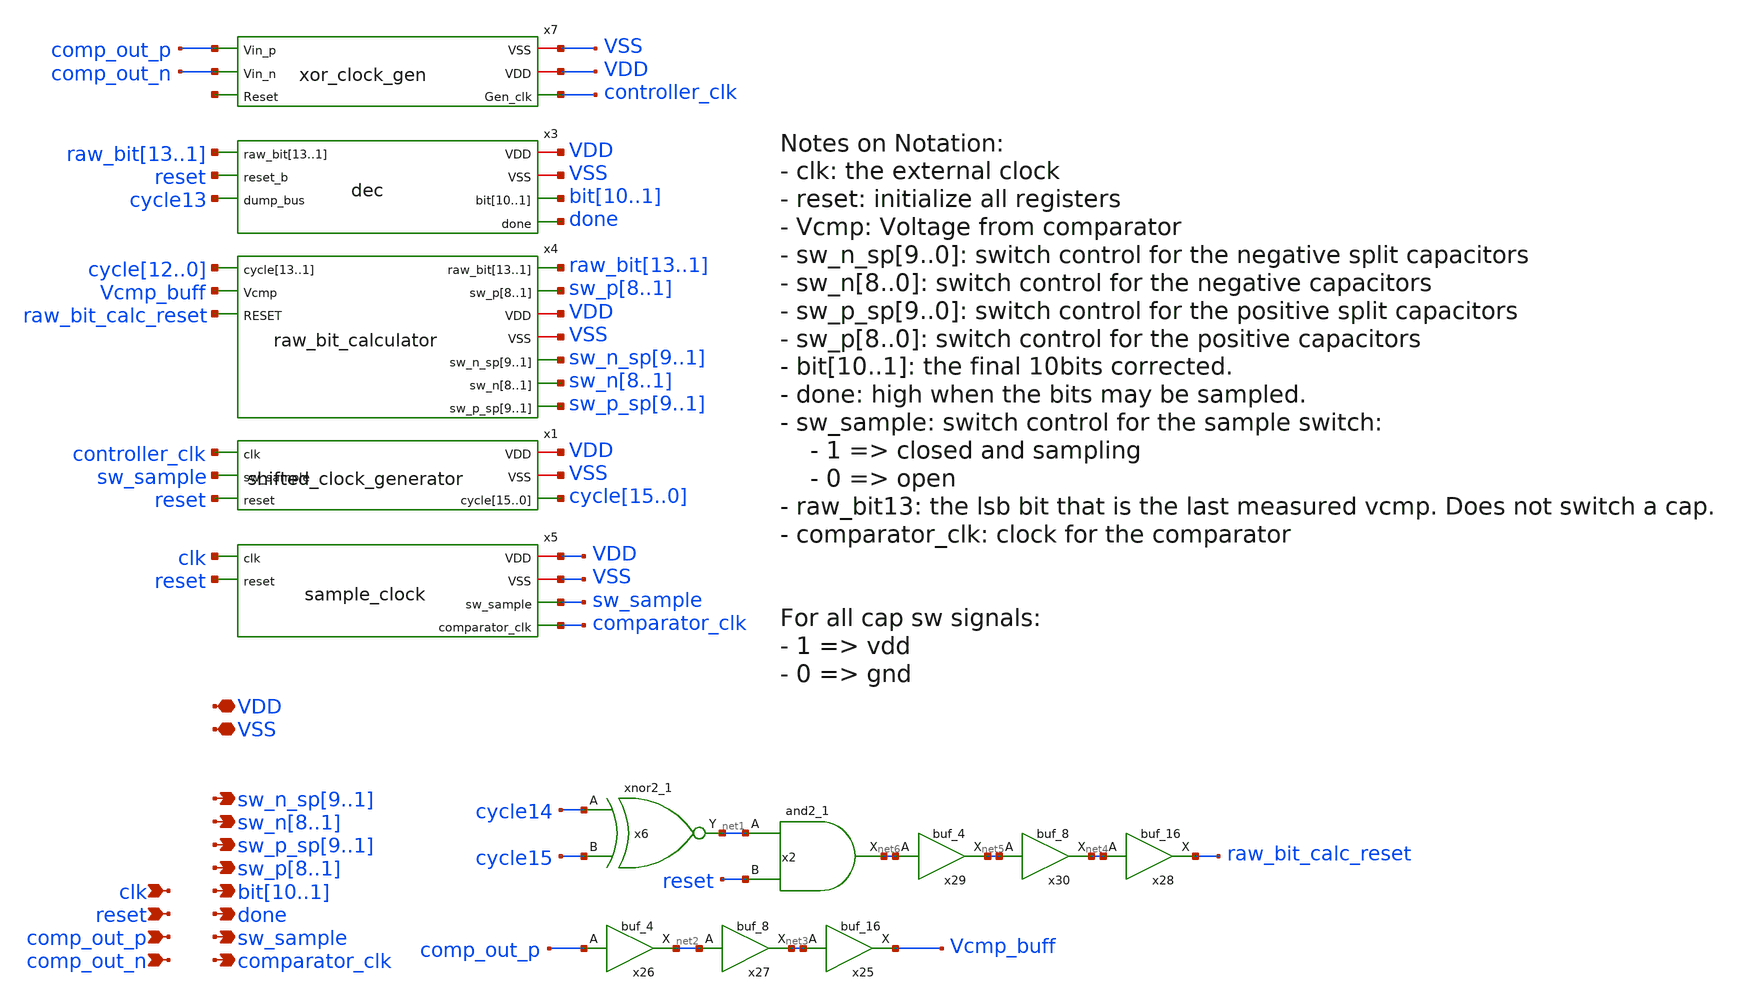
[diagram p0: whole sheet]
** sch_path: xschem/src/controller/controller.sch
**.subckt controller clk
*+ sw_n_sp9,sw_n_sp8,sw_n_sp7,sw_n_sp6,sw_n_sp5,sw_n_sp4,sw_n_sp3,sw_n_sp2,sw_n_sp1 VSS VDD reset sw_n8,sw_n7,sw_n6,sw_n5,sw_n4,sw_n3,sw_n2,sw_n1
*+ sw_p_sp9,sw_p_sp8,sw_p_sp7,sw_p_sp6,sw_p_sp5,sw_p_sp4,sw_p_sp3,sw_p_sp2,sw_p_sp1 sw_p8,sw_p7,sw_p6,sw_p5,sw_p4,sw_p3,sw_p2,sw_p1 bit10,bit9,bit8,bit7,bit6,bit5,bit4,bit3,bit2,bit1
*+ done sw_sample comparator_clk comp_out_p comp_out_n
*.ipin clk
*.opin sw_n_sp9,sw_n_sp8,sw_n_sp7,sw_n_sp6,sw_n_sp5,sw_n_sp4,sw_n_sp3,sw_n_sp2,sw_n_sp1
*.iopin VSS
*.iopin VDD
*.ipin reset
*.opin sw_n8,sw_n7,sw_n6,sw_n5,sw_n4,sw_n3,sw_n2,sw_n1
*.opin sw_p_sp9,sw_p_sp8,sw_p_sp7,sw_p_sp6,sw_p_sp5,sw_p_sp4,sw_p_sp3,sw_p_sp2,sw_p_sp1
*.opin sw_p8,sw_p7,sw_p6,sw_p5,sw_p4,sw_p3,sw_p2,sw_p1
*.opin bit10,bit9,bit8,bit7,bit6,bit5,bit4,bit3,bit2,bit1
*.opin done
*.opin sw_sample
*.opin comparator_clk
*.ipin comp_out_p
*.ipin comp_out_n
x3 VDD raw_bit13 raw_bit12 raw_bit11 raw_bit10 raw_bit9 raw_bit8 raw_bit7 raw_bit6 raw_bit5 raw_bit4
+ raw_bit3 raw_bit2 raw_bit1 VSS reset bit10 bit9 bit8 bit7 bit6 bit5 bit4 bit3 bit2 bit1 done cycle13 dec
x4 raw_bit13 raw_bit12 raw_bit11 raw_bit10 raw_bit9 raw_bit8 raw_bit7 raw_bit6 raw_bit5 raw_bit4
+ raw_bit3 raw_bit2 raw_bit1 cycle12 cycle11 cycle10 cycle9 cycle8 cycle7 cycle6 cycle5 cycle4 cycle3 cycle2
+ cycle1 cycle0 sw_p8 sw_p7 sw_p6 sw_p5 sw_p4 sw_p3 sw_p2 sw_p1 Vcmp_buff raw_bit_calc_reset VDD VSS
+ sw_n_sp9 sw_n_sp8 sw_n_sp7 sw_n_sp6 sw_n_sp5 sw_n_sp4 sw_n_sp3 sw_n_sp2 sw_n_sp1 sw_n8 sw_n7 sw_n6 sw_n5
+ sw_n4 sw_n3 sw_n2 sw_n1 sw_p_sp9 sw_p_sp8 sw_p_sp7 sw_p_sp6 sw_p_sp5 sw_p_sp4 sw_p_sp3 sw_p_sp2 sw_p_sp1
+ raw_bit_calculator
x1 VDD controller_clk sw_sample VSS reset cycle15 cycle14 cycle13 cycle12 cycle11 cycle10 cycle9
+ cycle8 cycle7 cycle6 cycle5 cycle4 cycle3 cycle2 cycle1 cycle0 shifted_clock_generator
x2 net1 reset VSS VSS VDD VDD net6 sky130_fd_sc_hd__and2_1
x6 cycle14 cycle15 VSS VSS VDD VDD net1 sky130_fd_sc_hd__xnor2_1
x25 net3 VSS VSS VDD VDD Vcmp_buff sky130_fd_sc_hd__buf_16
x26 comp_out_p VSS VSS VDD VDD net2 sky130_fd_sc_hd__buf_4
x27 net2 VSS VSS VDD VDD net3 sky130_fd_sc_hd__buf_8
x28 net4 VSS VSS VDD VDD raw_bit_calc_reset sky130_fd_sc_hd__buf_16
x29 net6 VSS VSS VDD VDD net5 sky130_fd_sc_hd__buf_4
x30 net5 VSS VSS VDD VDD net4 sky130_fd_sc_hd__buf_8
x5 VDD clk reset VSS sw_sample comparator_clk sample_clock
x7 VSS comp_out_p VDD comp_out_n controller_clk net7 xor_clock_gen
**.ends
.end
